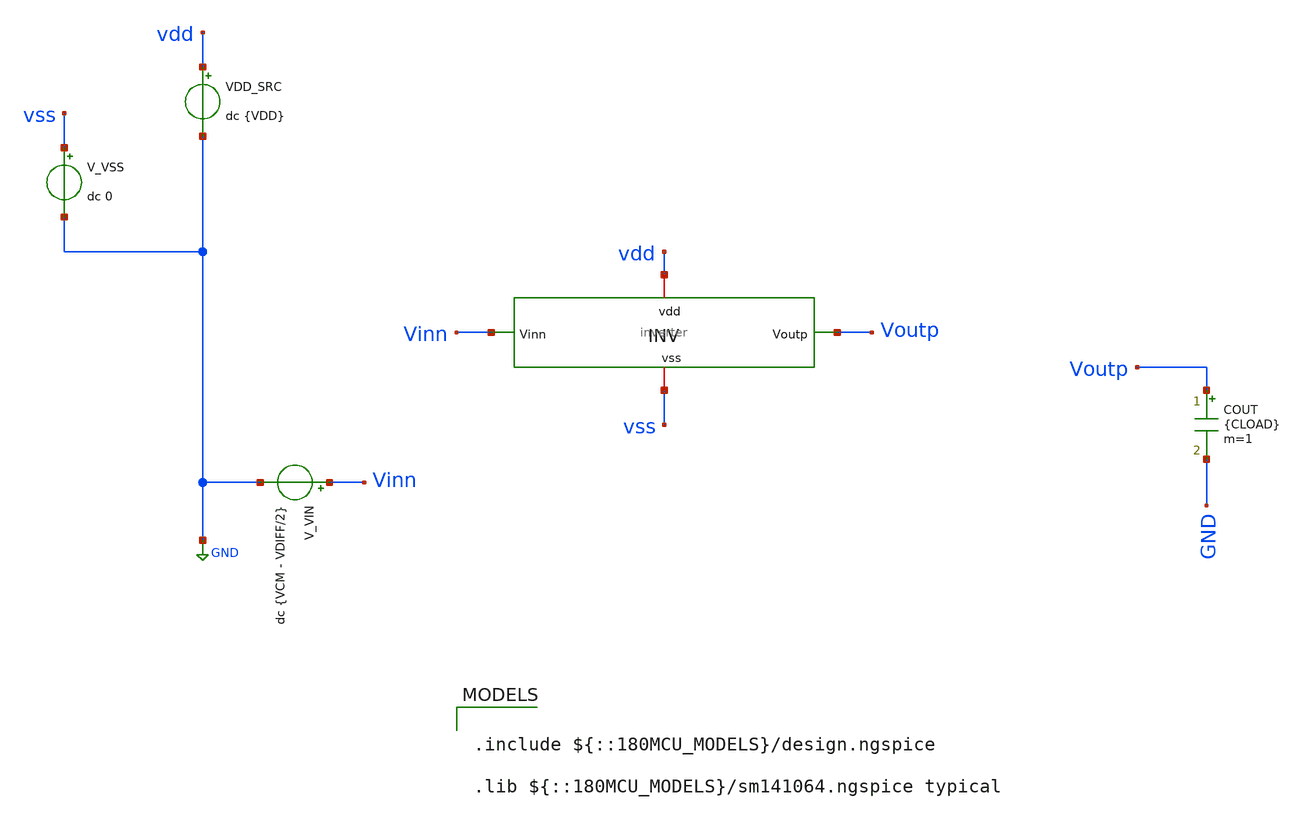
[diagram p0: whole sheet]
** sch_path: circuit_files/sar_adc_test/tb/inv_tb.sch
**.subckt inv_tb
V_VIN Vinn GND dc {VCM - VDIFF/2}
VDD_SRC vdd GND dc {VDD}
V_VSS vss GND dc 0
COUT Voutp GND {CLOAD} m=1
x2 vdd Vinn Voutp vss inverter
**** begin user architecture code

.include ${::180MCU_MODELS}/design.ngspice

.lib ${::180MCU_MODELS}/sm141064.ngspice typical







**** end user architecture code
**.ends

* expanding   symbol:  sar_adc_gf180/xschem/inverter.sym # of pins=4
** sym_path: circuit_files/sar_adc_test/xschem/inverter.sym
** sch_path: circuit_files/sar_adc_test/xschem/inverter.sch
.subckt inverter vdd Vinn Voutp vss
*.iopin vdd
*.iopin vss
*.ipin Vinn
*.opin Voutp
XM12 Voutp Vinn vss vss sg13_hv_nmos w=2u l=0.45u ng=1 m=1 mm_ok=1
XM16 Voutp Vinn vdd vdd sg13_hv_pmos w=2u l=0.4u ng=1 m=2 mm_ok=1
.ends

.GLOBAL GND
.end
